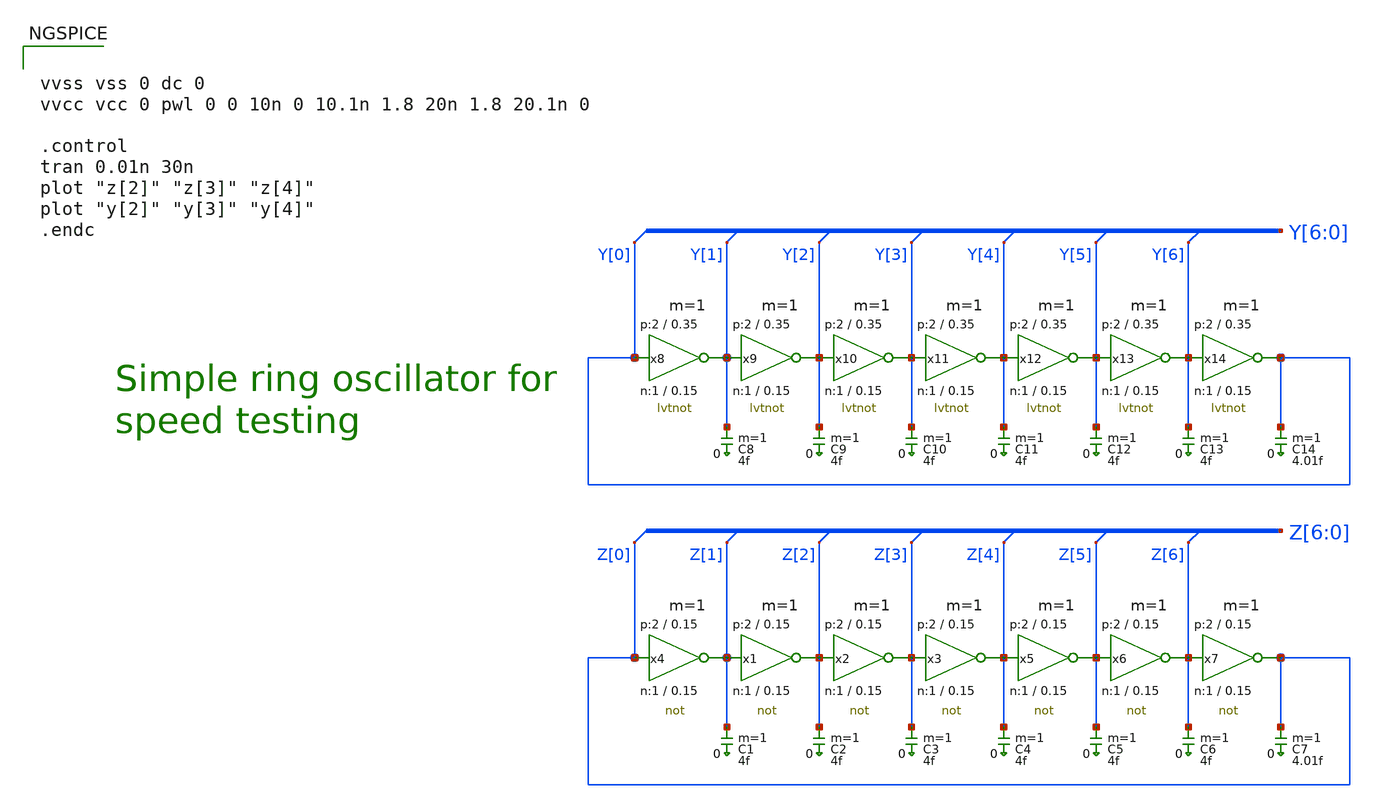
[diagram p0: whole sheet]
** sch_path: sky130_tests/test_inv.sch
* Copyright 2020 Stefan Frederik Schippers
* Licensed under the Apache License, Version 2.0 (the "License");
* you may not use this file except in compliance with the License.
* You may obtain a copy of the License at
* https://www.apache.org/licenses/LICENSE-2.0
* Unless required by applicable law or agreed to in writing, software
* distributed under the License is distributed on an "AS IS" BASIS,
* WITHOUT WARRANTIES OR CONDITIONS OF ANY KIND, either express or implied.
* See the License for the specific language governing permissions and
* limitations under the License.
* sky130_tests/not.sch:
* Copyright 2021 Stefan Frederik Schippers
**.subckt test_inv
C1 Z[1] 0 4f m=1
C2 Z[2] 0 4f m=1
C3 Z[3] 0 4f m=1
C4 Z[4] 0 4f m=1
C5 Z[5] 0 4f m=1
C6 Z[6] 0 4f m=1
C7 Z[0] 0 4.01f m=1
C8 Y[1] 0 4f m=1
C9 Y[2] 0 4f m=1
C10 Y[3] 0 4f m=1
C11 Y[4] 0 4f m=1
C12 Y[5] 0 4f m=1
C13 Y[6] 0 4f m=1
C14 Y[0] 0 4.01f m=1
x4 Z[1] Z[0] VCC VSS not W_N=1 L_N=0.15 W_P=2 L_P=0.15 m=1
x1 Z[2] Z[1] VCC VSS not W_N=1 L_N=0.15 W_P=2 L_P=0.15 m=1
x2 Z[3] Z[2] VCC VSS not W_N=1 L_N=0.15 W_P=2 L_P=0.15 m=1
x3 Z[4] Z[3] VCC VSS not W_N=1 L_N=0.15 W_P=2 L_P=0.15 m=1
x5 Z[5] Z[4] VCC VSS not W_N=1 L_N=0.15 W_P=2 L_P=0.15 m=1
x6 Z[6] Z[5] VCC VSS not W_N=1 L_N=0.15 W_P=2 L_P=0.15 m=1
x7 Z[0] Z[6] VCC VSS not W_N=1 L_N=0.15 W_P=2 L_P=0.15 m=1
x8 Y[1] Y[0] VCC VSS lvtnot W_N=1 L_N=0.15 W_P=2 L_P=0.35 m=1
x9 Y[2] Y[1] VCC VSS lvtnot W_N=1 L_N=0.15 W_P=2 L_P=0.35 m=1
x10 Y[3] Y[2] VCC VSS lvtnot W_N=1 L_N=0.15 W_P=2 L_P=0.35 m=1
x11 Y[4] Y[3] VCC VSS lvtnot W_N=1 L_N=0.15 W_P=2 L_P=0.35 m=1
x12 Y[5] Y[4] VCC VSS lvtnot W_N=1 L_N=0.15 W_P=2 L_P=0.35 m=1
x13 Y[6] Y[5] VCC VSS lvtnot W_N=1 L_N=0.15 W_P=2 L_P=0.35 m=1
x14 Y[0] Y[6] VCC VSS lvtnot W_N=1 L_N=0.15 W_P=2 L_P=0.35 m=1
**** begin user architecture code


vvss vss 0 dc 0
vvcc vcc 0 pwl 0 0 10n 0 10.1n 1.8 20n 1.8 20.1n 0

.control
tran 0.01n 30n
plot "z[2]" "z[3]" "z[4]"
plot "y[2]" "y[3]" "y[4]"
.endc


eval(
**** end user architecture code
**.ends

* expanding   symbol:  sky130_tests/not.sym # of pins=2
** sym_path: sky130_tests/not.sym
** sch_path: sky130_tests/not.sch
.subckt not y a VCCPIN VSSPIN     W_N=1 L_N=0.15 W_P=2 L_P=0.15
*.opin y
*.ipin a
XM1 DN a VSSPIN VSSPIN sky130_fd_pr__nfet_01v8 L=L_N W=W_N nf=1 ad='int((1 + 1)/2) * W_N / 1 * 0.29'
+ as='int((1 + 2)/2) * W_N / 1 * 0.29' pd='2*int((1 + 1)/2) * (W_N / 1 + 0.29)' ps='2*int((1 + 2)/2) * (W_N / 1 + 0.29)'
+ nrd='0.29 / W_N ' nrs='0.29 / W_N ' sa=0 sb=0 sd=0 mult=1 m=1
XM2 DP a VCCPIN VCCPIN sky130_fd_pr__pfet_01v8 L=L_P W=W_P nf=1 ad='int((nf+1)/2) * W/nf * 0.29' as='int((nf+2)/2) * W/nf * 0.29'
+ pd='2*int((nf+1)/2) * (W/nf + 0.29)' ps='2*int((nf+2)/2) * (W/nf + 0.29)' nrd='0.29 / W' nrs='0.29 / W'
+ sa=0 sb=0 sd=0 mult=1 m=1
Vmeas DP y 0
.save i(vmeas)
Vmeas1 y DN 0
.save i(vmeas1)
.save v(dp)
.save v(dn)
.ends


* expanding   symbol:  sky130_tests/lvtnot.sym # of pins=2
** sym_path: sky130_tests/lvtnot.sym
** sch_path: sky130_tests/lvtnot.sch
.subckt lvtnot y a VCCPIN VSSPIN     W_N=1 L_N=0.15 W_P=2 L_P=0.35
*.opin y
*.ipin a
XM1 y a VSSPIN VSSPIN sky130_fd_pr__nfet_01v8_lvt W=W_N L=L_N ad='W * 0.29' pd='2 * (W + 0.29)' as='W * 0.29'
+ ps='2 * (W + 0.29)' nrd='0.29 / W' nrs='0.29 / W' sa=0 sb=0 sd=0 nf=1 mult=1 m=1
XM2 y a VCCPIN VCCPIN sky130_fd_pr__pfet_01v8_lvt L=L_P W=W_P nf=1 ad='int((1 + 1)/2) * W_P / 1 * 0.29'
+ as='int((1 + 2)/2) * W_P / 1 * 0.29' pd='2*int((1 + 1)/2) * (W_P / 1 + 0.29)' ps='2*int((1 + 2)/2) * (W_P / 1 + 0.29)'
+ nrd='0.29 / W_P ' nrs='0.29 / W_P ' sa=0 sb=0 sd=0 mult=1 m=1
.ends

.end
